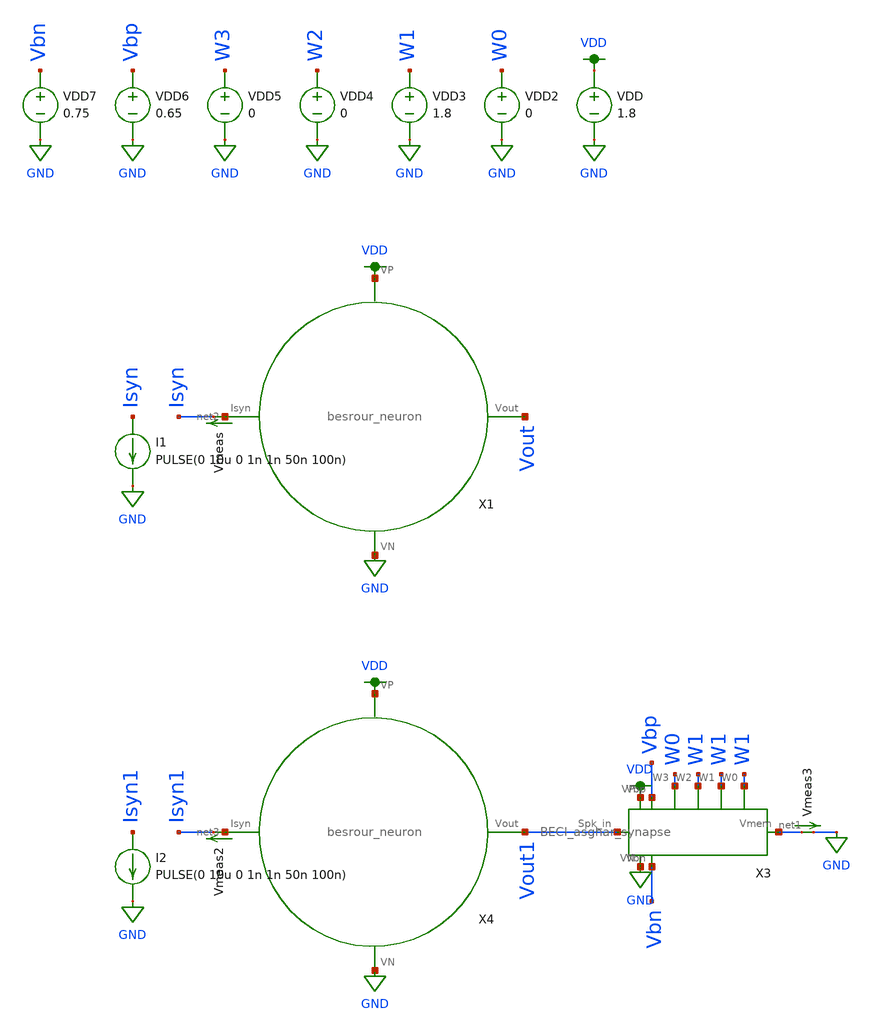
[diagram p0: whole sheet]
** sch_path: schematic/tran_neuron.sch
**.subckt tran_neuron
VDD VDD GND 1.8
I1 Isyn GND PULSE(0 10u 0 1n 1n 50n 100n)
Vmeas net2 Isyn 0
.save i(vmeas)
VDD2 W0 GND 0
VDD3 W1 GND 1.8
VDD4 W2 GND 0
VDD5 W3 GND 0
VDD6 Vbp GND 0.65
VDD7 Vbn GND 0.75
I2 Isyn1 GND PULSE(0 10u 0 1n 1n 50n 100n)
Vmeas2 net3 Isyn1 0
.save i(vmeas2)
Vmeas3 net1 GND 0
.save i(vmeas3)
X3 VDD GND Vout1 net1 W0 W1 W1 W1 Vbp Vbn BECI_asghar_synapse
X4 net3 Vout1 VDD GND besrour_neuron
X1 net2 Vout VDD GND besrour_neuron
**** begin user architecture code

.param W=12
.param L=0.5
.tran 0.1n 250n
.save all


.option wnflag=1
.param MC_SWITCH=0.0
.lib ~/skywater/skywater-pdk/libraries/sky130_fd_pr_ngspice/latest/models/sky130.lib.spice tt

**** end user architecture code
**.ends
.GLOBAL GND
.GLOBAL VDD
.end
